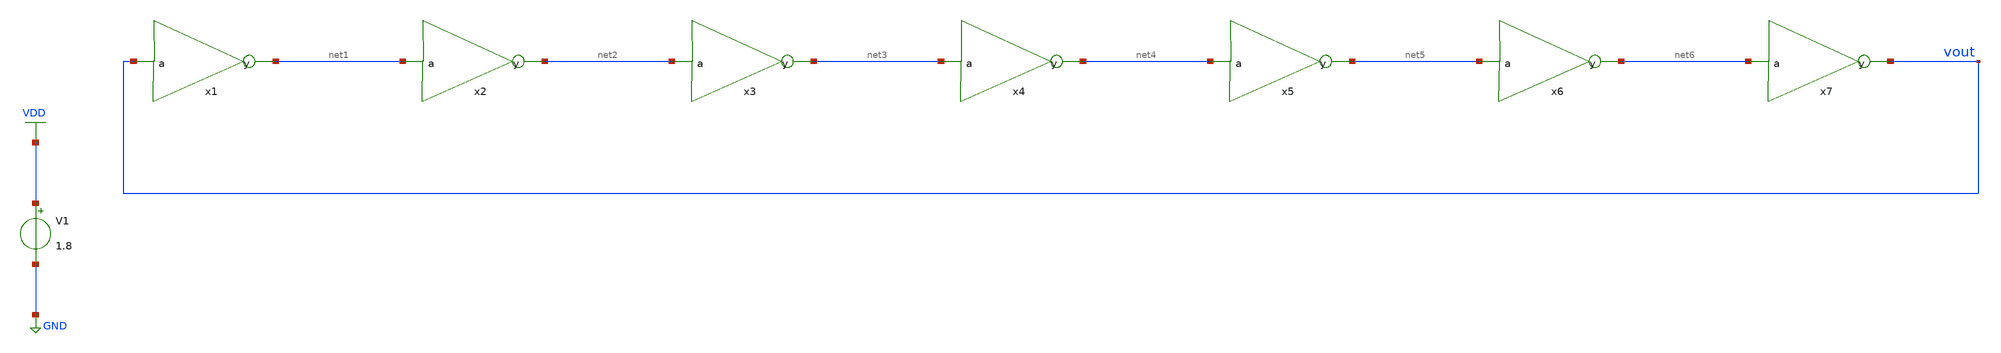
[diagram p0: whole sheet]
** sch_path: assignments/assignment3/assign2a.sch
**.subckt assign2a
x1 net1 vout inverter
x2 net2 net1 inverter
x3 net3 net2 inverter
x4 net4 net3 inverter
x5 net5 net4 inverter
x6 net6 net5 inverter
x7 vout net6 inverter
V1 VDD GND 1.8
**** begin user architecture code


.param VDDVal = 1.8
.param width_p = 0.84

* Force Vout to 0V at t=0 to kickstart the oscillation
.ic v(vout)=0

.control
* Run transient analysis for 5ns.
tran 1p 5n uic

* CORRECTED: Use 'WHEN' to grab the exact timestamp of the edges
meas tran t1 WHEN v(vout)=0.9 rise=4
meas tran t2 WHEN v(vout)=0.9 rise=5

* Calculate period and frequency (Frequency = 1 / Period)
let period = t2 - t1
let freq = 1 / period

* Print the results to the terminal
print period
print freq

* Plot the oscillating waveform
plot v(vout)
.endc


.lib $::SKYWATER_MODELS/sky130.lib.spice tt
**** end user architecture code
**.ends

* expanding   symbol:  inverter.sym # of pins=2
** sym_path: assignments/assignment3/inverter.sym
** sch_path: assignments/assignment3/inverter.sch
.subckt inverter y a
*.ipin a
*.opin y
XM1 y a GND GND sky130_fd_pr__nfet_01v8 L=0.15 W=0.42 nf=1 ad='int((nf+1)/2) * W/nf * 0.29' as='int((nf+2)/2) * W/nf * 0.29'
+ pd='2*int((nf+1)/2) * (W/nf + 0.29)' ps='2*int((nf+2)/2) * (W/nf + 0.29)' nrd='0.29 / W' nrs='0.29 / W'
+ sa=0 sb=0 sd=0 mult=1 m=1
XM2 y a VDD VDD sky130_fd_pr__pfet_01v8 L=0.15 W={width_p} nf=1 ad='int((nf+1)/2) * W/nf * 0.29' as='int((nf+2)/2) * W/nf * 0.29'
+ pd='2*int((nf+1)/2) * (W/nf + 0.29)' ps='2*int((nf+2)/2) * (W/nf + 0.29)' nrd='0.29 / W' nrs='0.29 / W'
+ sa=0 sb=0 sd=0 mult=1 m=1
.ends

.GLOBAL VDD
.GLOBAL GND
.end
